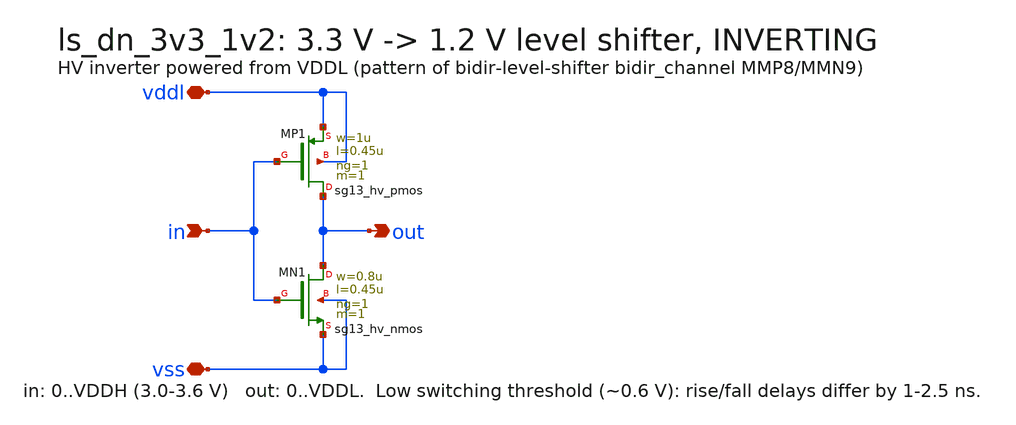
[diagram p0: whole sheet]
** sch_path: ls_pair/xschem/ls_dn_3v3_1v2.sch
**.subckt ls_dn_3v3_1v2 vss vddl out in
*.iopin vss
*.iopin vddl
*.opin out
*.ipin in
XMP1 out in vddl vddl sg13_hv_pmos w=1u l=0.45u ng=1 m=1 mm_ok=1
XMN1 out in vss vss sg13_hv_nmos w=0.8u l=0.45u ng=1 m=1 mm_ok=1
**.ends
.end
